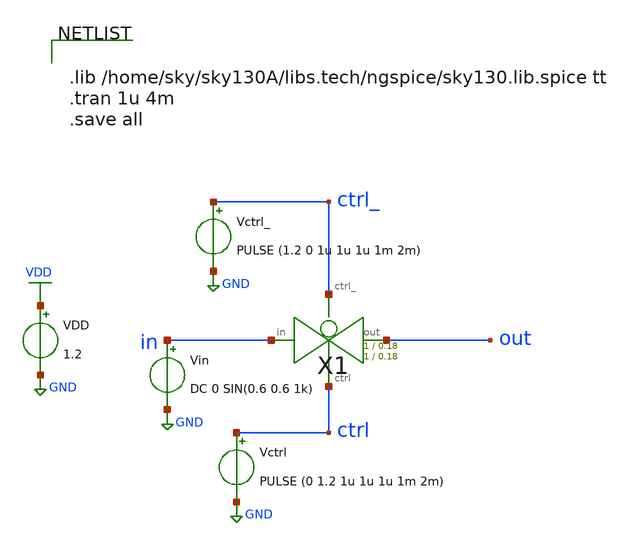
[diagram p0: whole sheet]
** sch_path: xschem/transmission_gate/transmission_gate_tb.sch
**.subckt transmission_gate_tb
X1 in out ctrl_ ctrl transmission_gate Wpmos=1 Lpmos=0.18 Wnmos=1 Lnmos=0.18
Vin in GND DC 0 SIN(0.6 0.6 1k)
VDD VDD GND 1.2
Vctrl ctrl GND PULSE (0 1.2 1u 1u 1u 1m 2m)
Vctrl_ ctrl_ GND PULSE (1.2 0 1u 1u 1u 1m 2m)
**** begin user architecture code


.lib /home/sky/sky130A/libs.tech/ngspice/sky130.lib.spice tt
.tran 1u 4m
.save all


**** end user architecture code
**.ends

* expanding   symbol:  transmission_gate.sym # of pins=4
** sym_path: xschem/transmission_gate/transmission_gate.sym
** sch_path: xschem/transmission_gate/transmission_gate.sch
.subckt transmission_gate in out ctrl_ ctrl  Wpmos=1 Lpmos=0.18 Wnmos=1 Lnmos=0.18
*.iopin in
*.iopin out
*.ipin ctrl_
*.ipin ctrl
XM1 in ctrl out GND sky130_fd_pr__nfet_01v8 L=Lnmos W=Wnmos nf=1 ad='int((nf+1)/2) * W/nf * 0.29' as='int((nf+2)/2) * W/nf * 0.29'
+ pd='2*int((nf+1)/2) * (W/nf + 0.29)' ps='2*int((nf+2)/2) * (W/nf + 0.29)' nrd='0.29 / W' nrs='0.29 / W'
+ sa=0 sb=0 sd=0 mult=1 m=1
XM2 out ctrl_ in VDD sky130_fd_pr__pfet_01v8 L=Lpmos W=Wpmos nf=1 ad='int((nf+1)/2) * W/nf * 0.29' as='int((nf+2)/2) * W/nf * 0.29'
+ pd='2*int((nf+1)/2) * (W/nf + 0.29)' ps='2*int((nf+2)/2) * (W/nf + 0.29)' nrd='0.29 / W' nrs='0.29 / W'
+ sa=0 sb=0 sd=0 mult=1 m=1
.ends

.GLOBAL VDD
.GLOBAL GND
.end
